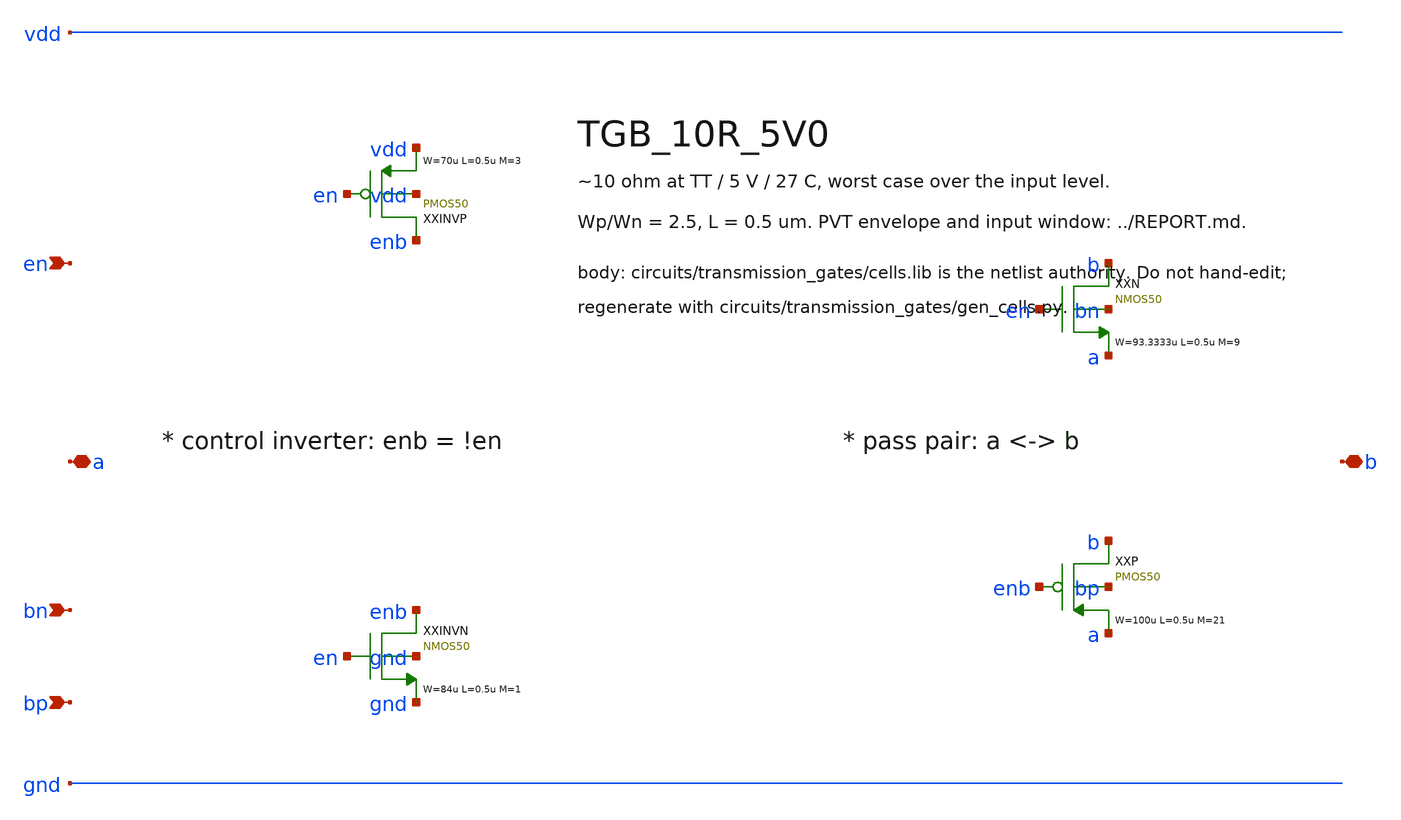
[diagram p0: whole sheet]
** sch_path: xschem/transmission_gates/TGB_10R_5V0.sch
**.subckt TGB_10R_5V0 a b en bn bp
*.iopin a
*.iopin b
*.ipin en
*.ipin bn
*.ipin bp
XXINVP enb en vdd vdd PMOS50 W=70u L=0.5u M=3 MM_SIGMA=0
XXINVN enb en gnd gnd NMOS50 W=84u L=0.5u M=1 MM_SIGMA=0
XXN b en a bn NMOS50 W=93.3333u L=0.5u M=9 MM_SIGMA=0
XXP b enb a bp PMOS50 W=100u L=0.5u M=21 MM_SIGMA=0
**.ends
.end
